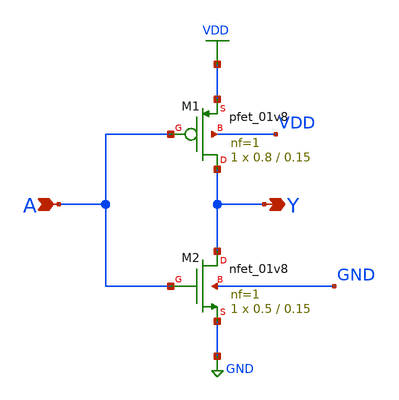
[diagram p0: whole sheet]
** sch_path: eng331lab_final/eng331lab_xschem/inv.sch
**.subckt inv A Y
*.ipin A
*.opin Y
XM1 Y A VDD VDD sky130_fd_pr__pfet_01v8 L=0.15 W=0.8 nf=1 ad='int((1 + 1)/2) * 0.8 / 1 * 0.29' as='int((1 + 2)/2) * 0.8 / 1 * 0.29'
+ pd='2*int((1 + 1)/2) * (0.8 / 1 + 0.29)' ps='2*int((1 + 2)/2) * (0.8 / 1 + 0.29)' nrd='0.29 / 0.8 ' nrs='0.29 / 0.8 '
+ sa=0 sb=0 sd=0 mult=1 m=1
XM2 Y A GND GND sky130_fd_pr__nfet_01v8 L=0.15 W=0.5 nf=1 ad='int((1 + 1)/2) * 0.5 / 1 * 0.29' as='int((1 + 2)/2) * 0.5 / 1 * 0.29'
+ pd='2*int((1 + 1)/2) * (0.5 / 1 + 0.29)' ps='2*int((1 + 2)/2) * (0.5 / 1 + 0.29)' nrd='0.29 / 0.5 ' nrs='0.29 / 0.5 '
+ sa=0 sb=0 sd=0 mult=1 m=1
**.ends
.GLOBAL VDD
.GLOBAL GND
.end
